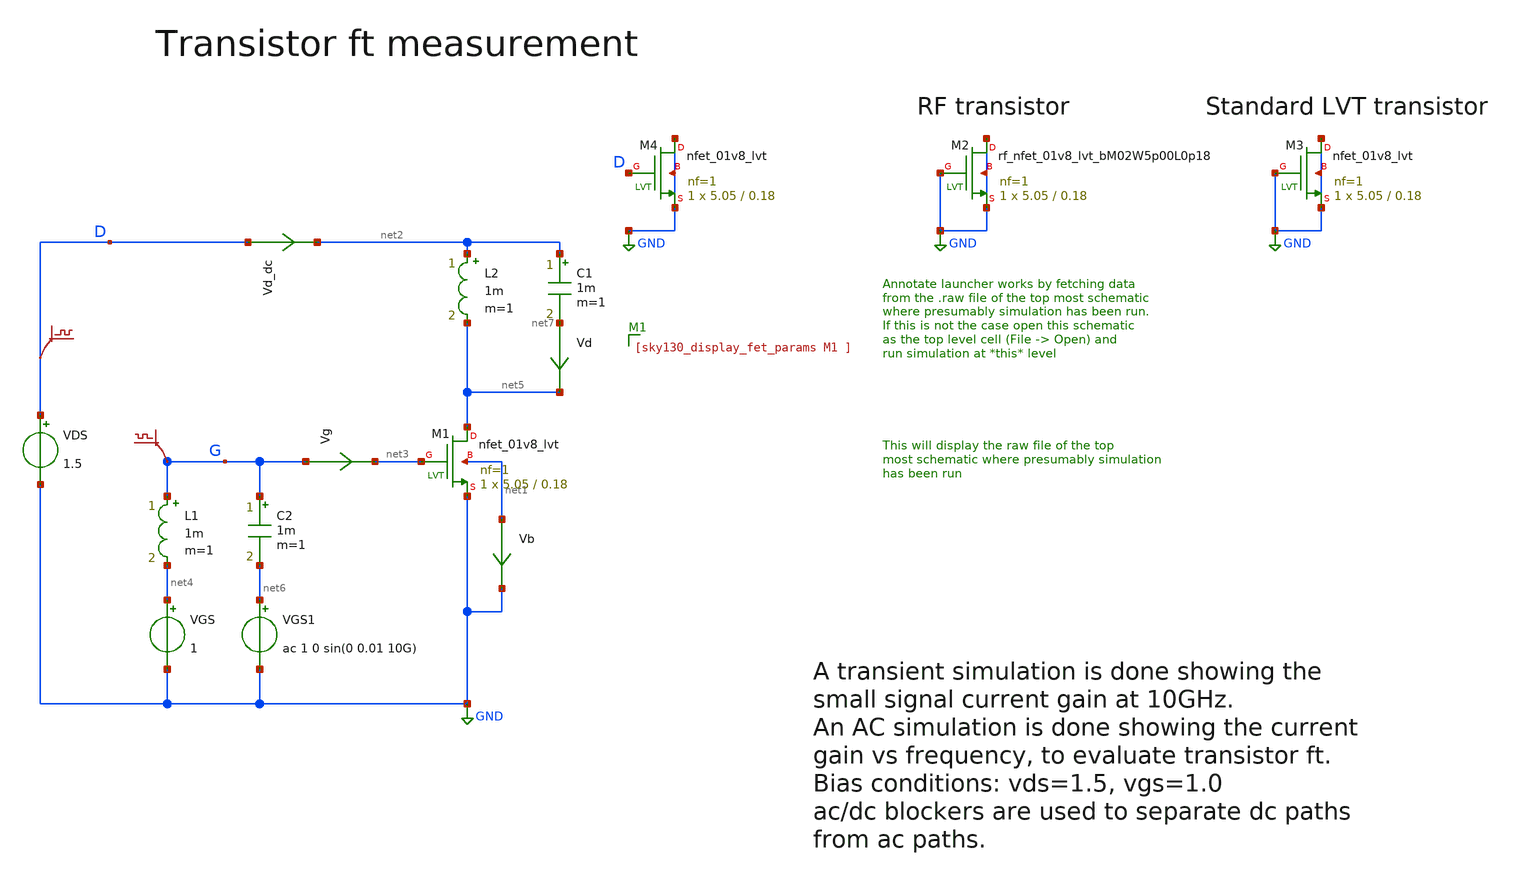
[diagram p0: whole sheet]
** sch_path: sky130A/xschem_libs/sky130_tests/tb_ft_test_2/schematic/tb_ft_test_2.sch
* Copyright 2021 Stefan Frederik Schippers
* Licensed under the Apache License, Version 2.0 (the "License");
* you may not use this file except in compliance with the License.
* You may obtain a copy of the License at
* https://www.apache.org/licenses/LICENSE-2.0
* Unless required by applicable law or agreed to in writing, software
* distributed under the License is distributed on an "AS IS" BASIS,
* WITHOUT WARRANTIES OR CONDITIONS OF ANY KIND, either express or implied.
* See the License for the specific language governing permissions and
* limitations under the License.
**.subckt tb_ft_test_2
VDS D GND 1.5
VGS net4 GND 1
Vd net7 net5 0
.save i(vd)
L1 G net4 1m m=1
Vg G net3 0
.save i(vg)
L2 net2 net5 1m m=1
C1 net2 net7 1m m=1
C2 G net6 1m m=1
VGS1 net6 GND ac 1 0 sin(0 0.01 10G)
Vd_dc D net2 0
.save i(vd_dc)
.save v(g)
.save v(d)
Vb net1 GND 0
.save i(vb)
XM2 GND GND GND GND sky130_fd_pr__rf_nfet_01v8_lvt_bM02W5p00L0p18 L=0.18 W=5.05 nf=1 ad='int((1 + 1)/2) * 5.05 / 1 * 0.29'
+ as='int((1 + 2)/2) * 5.05 / 1 * 0.29' pd='2*int((1 + 1)/2) * (5.05 / 1 + 0.29)' ps='2*int((1 + 2)/2) * (5.05 / 1 + 0.29)'
+ nrd='0.29 / 5.05 ' nrs='0.29 / 5.05 ' sa=0 sb=0 sd=0 mult=1 m=1
XM3 GND GND GND GND sky130_fd_pr__nfet_01v8_lvt L=0.18 W=5.05 nf=1 ad='int((1 + 1)/2) * 5.05 / 1 * 0.29'
+ as='int((1 + 2)/2) * 5.05 / 1 * 0.29' pd='2*int((1 + 1)/2) * (5.05 / 1 + 0.29)' ps='2*int((1 + 2)/2) * (5.05 / 1 + 0.29)'
+ nrd='0.29 / 5.05 ' nrs='0.29 / 5.05 ' sa=0 sb=0 sd=0 mult=1 m=1
XM1 net5 net3 GND net1 sky130_fd_pr__nfet_01v8_lvt L=0.18 W=5.05 nf=1 ad='int((1 + 1)/2) * 5.05 / 1 * 0.29'
+ as='int((1 + 2)/2) * 5.05 / 1 * 0.29' pd='2*int((1 + 1)/2) * (5.05 / 1 + 0.29)' ps='2*int((1 + 2)/2) * (5.05 / 1 + 0.29)'
+ nrd='0.29 / 5.05 ' nrs='0.29 / 5.05 ' sa=0 sb=0 sd=0 mult=1 m=1
XM4 GND D GND GND sky130_fd_pr__nfet_01v8_lvt L=0.18 W=5.05 nf=1 ad='int((1 + 1)/2) * 5.05 / 1 * 0.29'
+ as='int((1 + 2)/2) * 5.05 / 1 * 0.29' pd='2*int((1 + 1)/2) * (5.05 / 1 + 0.29)' ps='2*int((1 + 2)/2) * (5.05 / 1 + 0.29)'
+ nrd='0.29 / 5.05 ' nrs='0.29 / 5.05 ' sa=0 sb=0 sd=0 mult=1 m=1
**** begin user architecture code


* this experimental option enables mos model bin
* selection based on W/NF instead of W
.option wnflag=1
.options method=gear savecurrents
.save all
.include tb_ft_test_2.save
.control
  save all
* save @m.xm1.msky130_fd_pr__rf_nfet_01v8_lvt_bm02w5p00l0p18[gm]
*  save @m.xm1.msky130_fd_pr__nfet_01v8_lvt[gm]
  op
  write tb_ft_test_2.raw
  tran 0.001n 2n
  set appendwrite
  write tb_ft_test_2.raw
  ac dec 10 1000 1000G
  set appendwrite
  write tb_ft_test_2.raw
  setplot tran1
  plot i(vg) i(vd)
  setplot ac1
  plot db(i(vd)/i(vg))
.endc



** opencircuitdesign pdks install
.lib $::SKYWATER_MODELS/sky130.lib.spice tt

**** end user architecture code
**.ends
.GLOBAL GND
.end
